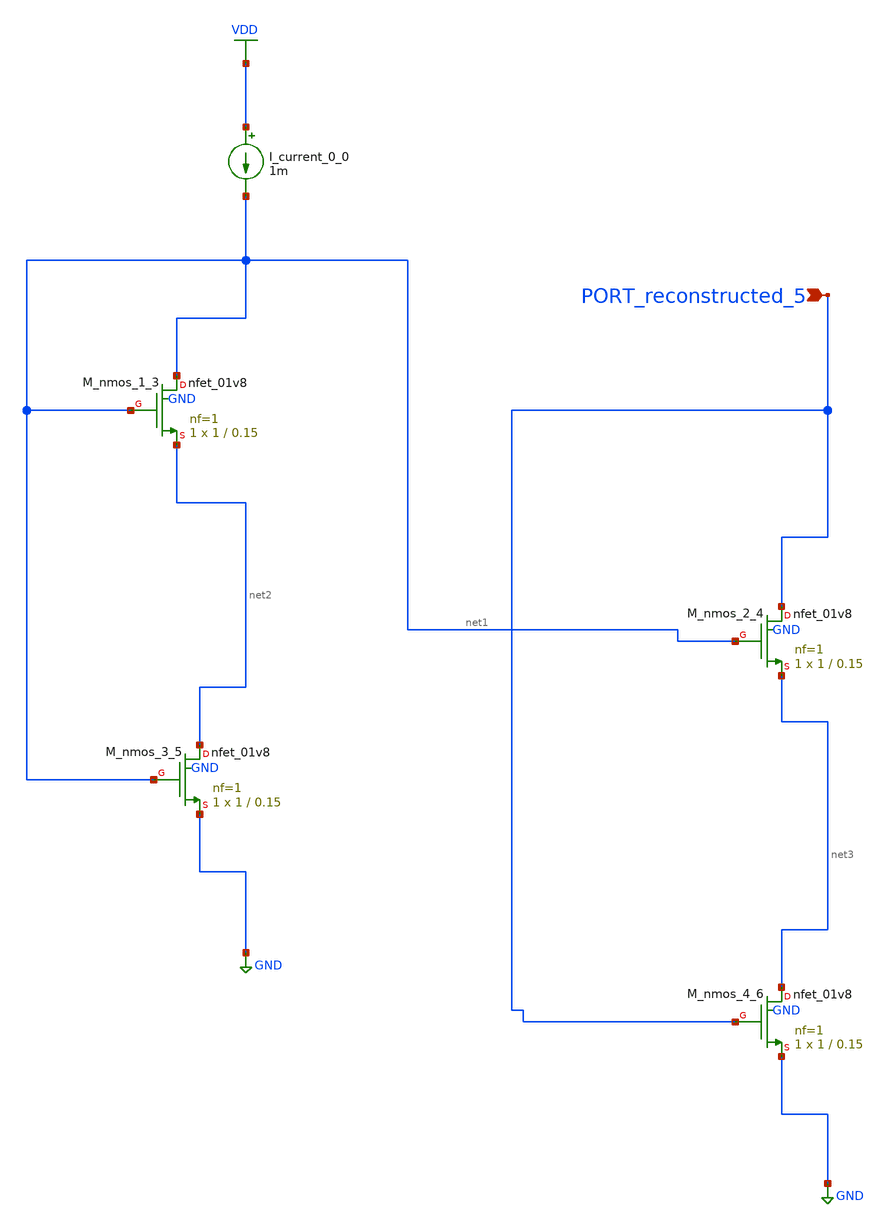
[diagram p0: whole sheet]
** sch_path: schematics/AMSNet/266.sch
**.subckt 266 PORT_reconstructed_5
*.ipin PORT_reconstructed_5
I_current_0_0 VDD net1 1m
XM_nmos_1_3 net1 net1 net2 GND sky130_fd_pr__nfet_01v8 L=0.15 W=1 nf=1 ad='int((1 + 1)/2) * 1 / 1 * 0.29'
+ as='int((1 + 2)/2) * 1 / 1 * 0.29' pd='2*int((1 + 1)/2) * (1 / 1 + 0.29)' ps='2*int((1 + 2)/2) * (1 / 1 + 0.29)'
+ nrd='0.29 / 1 ' nrs='0.29 / 1 ' sa=0 sb=0 sd=0 mult=1 m=1
XM_nmos_2_4 PORT_reconstructed_5 net1 net3 GND sky130_fd_pr__nfet_01v8 L=0.15 W=1 nf=1 ad='int((1 + 1)/2) * 1 / 1 * 0.29'
+ as='int((1 + 2)/2) * 1 / 1 * 0.29' pd='2*int((1 + 1)/2) * (1 / 1 + 0.29)' ps='2*int((1 + 2)/2) * (1 / 1 + 0.29)'
+ nrd='0.29 / 1 ' nrs='0.29 / 1 ' sa=0 sb=0 sd=0 mult=1 m=1
XM_nmos_3_5 net2 net1 GND GND sky130_fd_pr__nfet_01v8 L=0.15 W=1 nf=1 ad='int((1 + 1)/2) * 1 / 1 * 0.29'
+ as='int((1 + 2)/2) * 1 / 1 * 0.29' pd='2*int((1 + 1)/2) * (1 / 1 + 0.29)' ps='2*int((1 + 2)/2) * (1 / 1 + 0.29)'
+ nrd='0.29 / 1 ' nrs='0.29 / 1 ' sa=0 sb=0 sd=0 mult=1 m=1
XM_nmos_4_6 net3 PORT_reconstructed_5 GND GND sky130_fd_pr__nfet_01v8 L=0.15 W=1 nf=1 ad='int((1 + 1)/2) * 1 / 1 * 0.29'
+ as='int((1 + 2)/2) * 1 / 1 * 0.29' pd='2*int((1 + 1)/2) * (1 / 1 + 0.29)' ps='2*int((1 + 2)/2) * (1 / 1 + 0.29)'
+ nrd='0.29 / 1 ' nrs='0.29 / 1 ' sa=0 sb=0 sd=0 mult=1 m=1
**.ends
.GLOBAL GND
.GLOBAL VDD
.end
